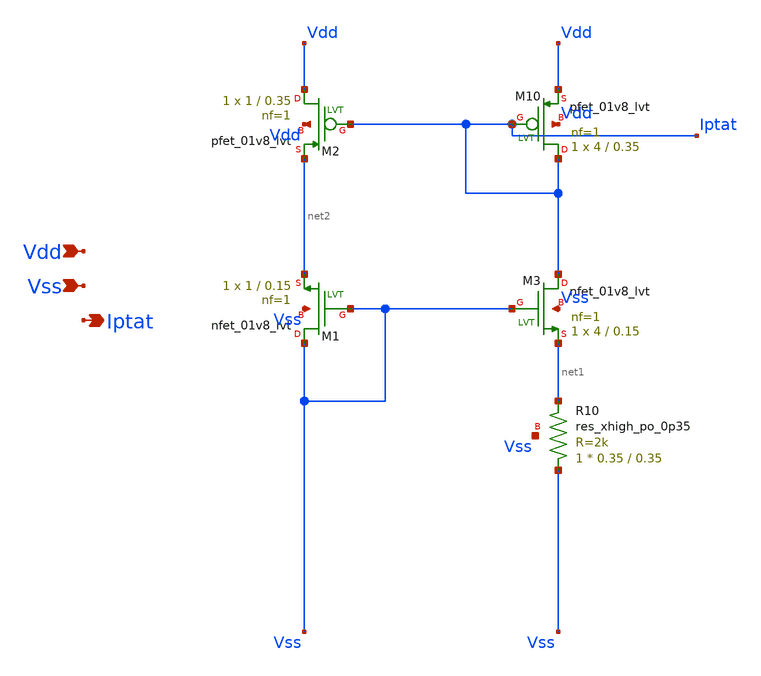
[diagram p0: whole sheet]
** sch_path: tt10-hdl/tt_um_test_commit/xschem/T2/biasGen/PTAT/carsten-wulff_ptat.sch
**.subckt carsten-wulff_ptat Vdd Vss Iptat
*.ipin Vdd
*.ipin Vss
*.opin Iptat
XM10 Iptat Iptat Vdd Vdd sky130_fd_pr__pfet_01v8_lvt L=0.35 W=4 nf=1 ad='int((1 + 1)/2) * 4 / 1 * 0.29'
+ as='int((1 + 2)/2) * 4 / 1 * 0.29' pd='2*int((1 + 1)/2) * (4 / 1 + 0.29)' ps='2*int((1 + 2)/2) * (4 / 1 + 0.29)'
+ nrd='0.29 / 4 ' nrs='0.29 / 4 ' sa=0 sb=0 sd=0 mult=1 m=1
XM1 Vss Vss net2 Vss sky130_fd_pr__nfet_01v8_lvt L=0.15 W=1 nf=1 ad='int((1 + 1)/2) * 1 / 1 * 0.29' as='int((1 + 2)/2) * 1 / 1 * 0.29'
+ pd='2*int((1 + 1)/2) * (1 / 1 + 0.29)' ps='2*int((1 + 2)/2) * (1 / 1 + 0.29)' nrd='0.29 / 1 ' nrs='0.29 / 1 '
+ sa=0 sb=0 sd=0 mult=1 m=1
XR10 Vss net1 Vss sky130_fd_pr__res_xhigh_po_0p35 L=0.35 mult=1 m=1
XM2 Vdd Iptat net2 Vdd sky130_fd_pr__pfet_01v8_lvt L=0.35 W=1 nf=1 ad='int((1 + 1)/2) * 1 / 1 * 0.29'
+ as='int((1 + 2)/2) * 1 / 1 * 0.29' pd='2*int((1 + 1)/2) * (1 / 1 + 0.29)' ps='2*int((1 + 2)/2) * (1 / 1 + 0.29)'
+ nrd='0.29 / 1 ' nrs='0.29 / 1 ' sa=0 sb=0 sd=0 mult=1 m=1
XM3 Iptat Vss net1 Vss sky130_fd_pr__nfet_01v8_lvt L=0.15 W=4 nf=1 ad='int((1 + 1)/2) * 4 / 1 * 0.29'
+ as='int((1 + 2)/2) * 4 / 1 * 0.29' pd='2*int((1 + 1)/2) * (4 / 1 + 0.29)' ps='2*int((1 + 2)/2) * (4 / 1 + 0.29)'
+ nrd='0.29 / 4 ' nrs='0.29 / 4 ' sa=0 sb=0 sd=0 mult=1 m=1
**.ends
.end
